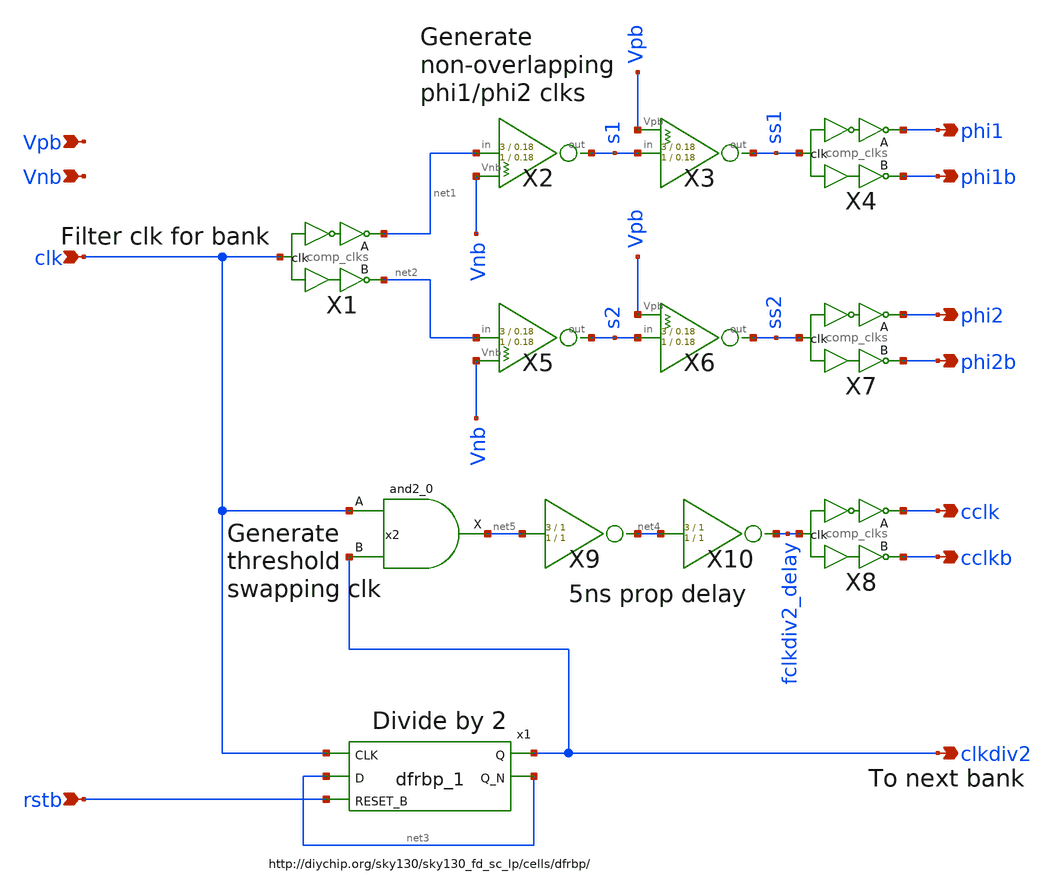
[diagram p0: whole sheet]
** sch_path: xschem/clkgen/filter_clkgen.sch
**.subckt filter_clkgen clk rstb phi1 phi1b phi2 phi2b cclk cclkb clkdiv2 Vpb Vnb
*.ipin clk
*.ipin rstb
*.opin phi1
*.opin phi1b
*.opin phi2
*.opin phi2b
*.opin cclk
*.opin cclkb
*.opin clkdiv2
*.ipin Vpb
*.ipin Vnb
X6 s2 ss2 Vpb inv_weak_pullup Wpmos=3 Lpmos=0.18 Wnmos=1 Lnmos=0.18
X5 net2 s2 Vnb inv_weak_pulldown Wpmos=3 Lpmos=0.18 Wnmos=1 Lnmos=0.18
X7 ss2 phi2 phi2b comp_clks Wpmos=3 Lpmos=0.18 Wnmos=1 Lnmos=0.18
X1 clk net1 net2 comp_clks Wpmos=3 Lpmos=0.18 Wnmos=1 Lnmos=0.18
X3 s1 ss1 Vpb inv_weak_pullup Wpmos=3 Lpmos=0.18 Wnmos=1 Lnmos=0.18
X2 net1 s1 Vnb inv_weak_pulldown Wpmos=3 Lpmos=0.18 Wnmos=1 Lnmos=0.18
X4 ss1 phi1 phi1b comp_clks Wpmos=3 Lpmos=0.18 Wnmos=1 Lnmos=0.18
x1 clk net3 rstb gnd gnd vdd vdd clkdiv2 net3 sky130_fd_sc_lp__dfrbp_1
x2 clk clkdiv2 gnd gnd vdd vdd net5 sky130_fd_sc_lp__and2_0
X8 fclkdiv2_delay cclk cclkb comp_clks Wpmos=3 Lpmos=0.18 Wnmos=1 Lnmos=0.18
X9 net5 net4 inv Wpmos=3 Lpmos=1 Wnmos=1 Lnmos=1
X10 net4 fclkdiv2_delay inv Wpmos=3 Lpmos=1 Wnmos=1 Lnmos=1
**.ends
.end
